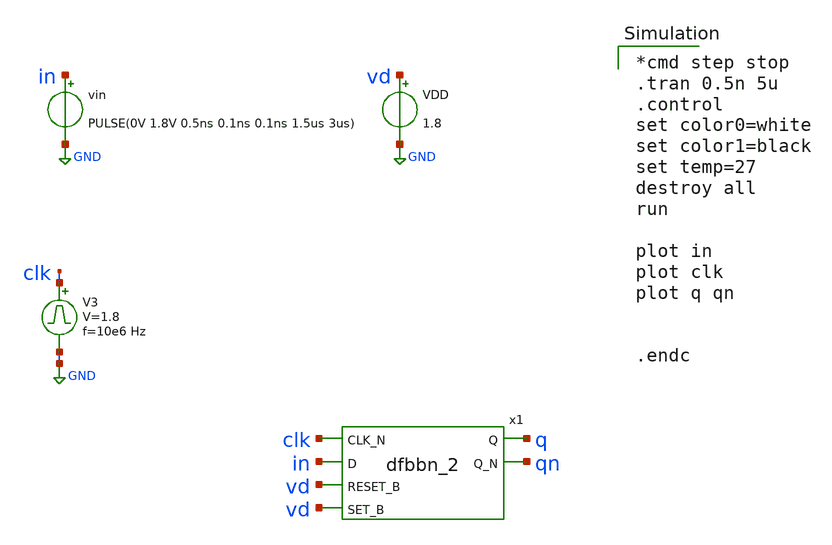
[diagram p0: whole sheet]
** sch_path: mag/sigma-delta_modulator/xschem/dff_tb-tran.sch
* Copyright 2020 Stefan Frederik Schippers
* Licensed under the Apache License, Version 2.0 (the "License");
* you may not use this file except in compliance with the License.
* You may obtain a copy of the License at
* https://www.apache.org/licenses/LICENSE-2.0
* Unless required by applicable law or agreed to in writing, software
* distributed under the License is distributed on an "AS IS" BASIS,
* WITHOUT WARRANTIES OR CONDITIONS OF ANY KIND, either express or implied.
* See the License for the specific language governing permissions and
* limitations under the License.
**.subckt dff_tb-tran
VDD vd GND 1.8
vin in GND PULSE(0V 1.8V 0.5ns 0.1ns 0.1ns 1.5us 3us)
x1 clk in vd vd GND GND VD VD q qn sky130_fd_sc_hd__dfbbn_2
V3 clk GND pulse 0 1.8 '0.495/ 10e6 ' '0.01/10e6 ' '0.01/10e6 ' '0.49/10e6 ' '1/10e6 '
**** begin user architecture code

*cmd step stop
.tran 0.5n 5u
.control
set color0=white
set color1=black
set temp=27
destroy all
run

plot in
plot clk
plot q qn


.endc

 .lib $::SKYWATER_MODELS/sky130.lib.spice tt
.include $::SKYWATER_STDCELLS/sky130_fd_sc_hd.spice

**** end user architecture code
**.ends
.GLOBAL GND
.end
